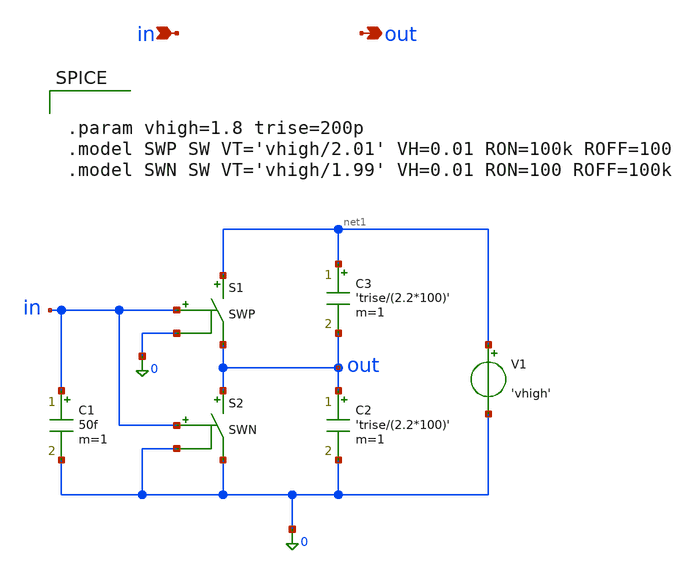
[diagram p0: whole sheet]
** sch_path: Xschem/sky130A/gate_not.sch
**.subckt gate_not in out
*.ipin in
*.opin out
C2 out 0 'trise/(2.2*100)' m=1
S1 net1 out in 0 SWP
S2 out 0 in 0 SWN
V1 net1 0 'vhigh'
C1 in 0 50f m=1
C3 net1 out 'trise/(2.2*100)' m=1
**** begin user architecture code


.param vhigh=1.8 trise=200p
.model SWP SW VT='vhigh/2.01' VH=0.01 RON=100k ROFF=100
.model SWN SW VT='vhigh/1.99' VH=0.01 RON=100 ROFF=100k


**** end user architecture code
**.ends
**** begin user architecture code
.MODEL SW1 SW   VT=0.9 VH=0.01  RON=0.01 ROFF=10G
**** end user architecture code
.end
